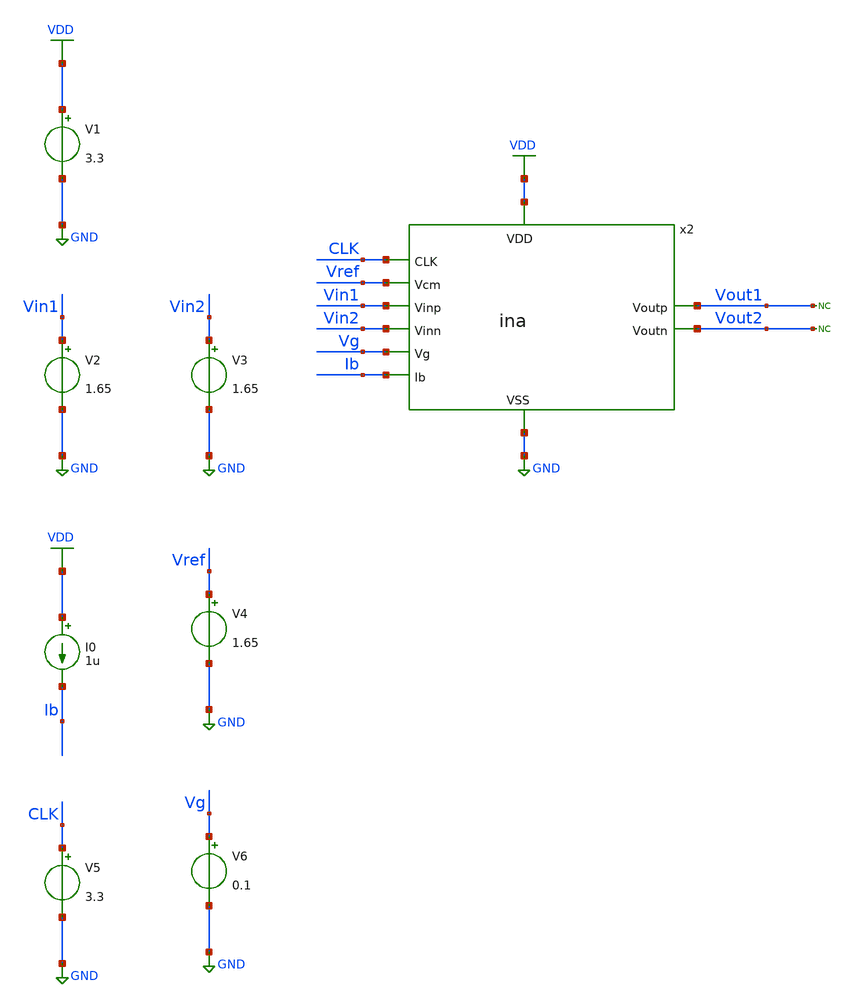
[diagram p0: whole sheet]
** sch_path: designs/libs/tb_ina/tb_ina_ac/tb_ina_ac.sch
**.subckt tb_ina_ac
V1 VDD GND 3.3
V2 Vin1 GND 1.65
V3 Vin2 GND 1.65
I0 VDD Ib 1u
V4 Vref GND 1.65
x2 Vg VDD Vin1 Vin2 CLK Vout1 Vout2 GND Vref Ib ina
V5 CLK GND 3.3
V6 Vg GND 0.1
* noconn Vout1
* noconn Vout2
**** begin user architecture code

.include $::180MCU_MODELS/design.ngspice
.lib $::180MCU_MODELS/sm141064.ngspice typical
.lib $::180MCU_MODELS/sm141064.ngspice cap_mim
.lib $::180MCU_MODELS/sm141064.ngspice moscap_typical
.lib $::180MCU_MODELS/sm141064.ngspice mimcap_typical
.lib $::180MCU_MODELS/sm141064.ngspice res_typical
* .lib $::180MCU_MODELS/sm141064.ngspice res_statistical
* ngspice commands




.control
save all

run
set color0 = white

*************************************
** PARAMETERS
*************************************

let Vdd  = 3.3
let Vcm  = 1.65
let Ibias = 2u
let Vg  = 0.1

*************************************
** CHOPPER PARAMETERS
*************************************

let fchop = 4k
let tper = 1/fchop
let ton = tper/2
let tr = 10n
let tf = 10n

*************************************
** SOURCES
*************************************

alter @V1[DC] = $&Vdd
alter @V2[DC] = $&Vcm
alter @V3[DC] = $&Vcm
alter @V2[ACMAG] = 0.5
alter @V3[ACMAG] = -0.5
alter @V4[DC] = $&Vcm
alter @I0[DC] = $&Ibias
alter @V5[PULSE] = [ 0 $&Vdd 0 $&tr $&tf $&ton $&tper 0 ]
alter @V6[DC] = $&Vg

*************************************
** AC SIMULATION
*************************************

ac dec 100 0.01 10G

*************************************
** MEASUREMENTS
*************************************

let vout_diff = v(Vout1)-v(Vout2)
let vin_diff  = v(Vin1)-v(Vin2)
let Av = vout_diff/vin_diff
let gain_db = db(Av)
meas ac A0 FIND gain_db AT=10
let A0_3dB = A0 - 3
meas ac fL WHEN gain_db=A0_3dB CROSS=1
meas ac fH WHEN gain_db=A0_3dB CROSS=2
let BW = fH - fL
meas ac UGF WHEN gain_db=0
print A0
print BW
print UGF

*************************************
** PLOTS
*************************************

plot gain_db

*************************************
** SAVE
*************************************

write tb_ina_ac.raw

.endc
* ngspice commands



**** end user architecture code
**.ends
.GLOBAL GND
.GLOBAL VDD
.end
